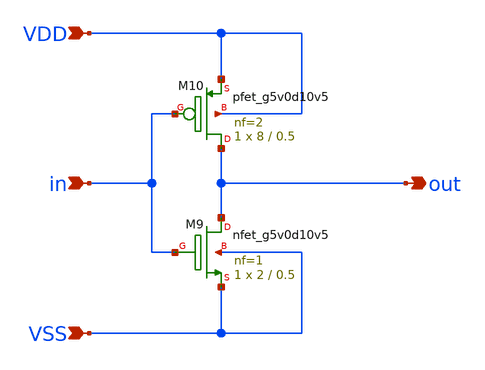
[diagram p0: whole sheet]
** sch_path: example/ana/inv.sch
**.subckt inv in out VDD VSS
*.ipin in
*.opin out
*.ipin VDD
*.ipin VSS
XM10 out in VDD VDD sky130_fd_pr__pfet_g5v0d10v5 L=0.5 W=8 nf=2 ad='int((2 + 1)/2) * 8 / 2 * 0.29' as='int((2 + 2)/2) * 8 / 2 * 0.29'
+ pd='2*int((2 + 1)/2) * (8 / 2 + 0.29)' ps='2*int((2 + 2)/2) * (8 / 2 + 0.29)' nrd='0.29 / 8 ' nrs='0.29 / 8 '
+ sa=0 sb=0 sd=0 mult=1 m=1
XM9 out in VSS VSS sky130_fd_pr__nfet_g5v0d10v5 L=0.5 W=2 nf=1 ad='int((1 + 1)/2) * 2 / 1 * 0.29' as='int((1 + 2)/2) * 2 / 1 * 0.29'
+ pd='2*int((1 + 1)/2) * (2 / 1 + 0.29)' ps='2*int((1 + 2)/2) * (2 / 1 + 0.29)' nrd='0.29 / 2 ' nrs='0.29 / 2 '
+ sa=0 sb=0 sd=0 mult=1 m=1
**.ends
.end
